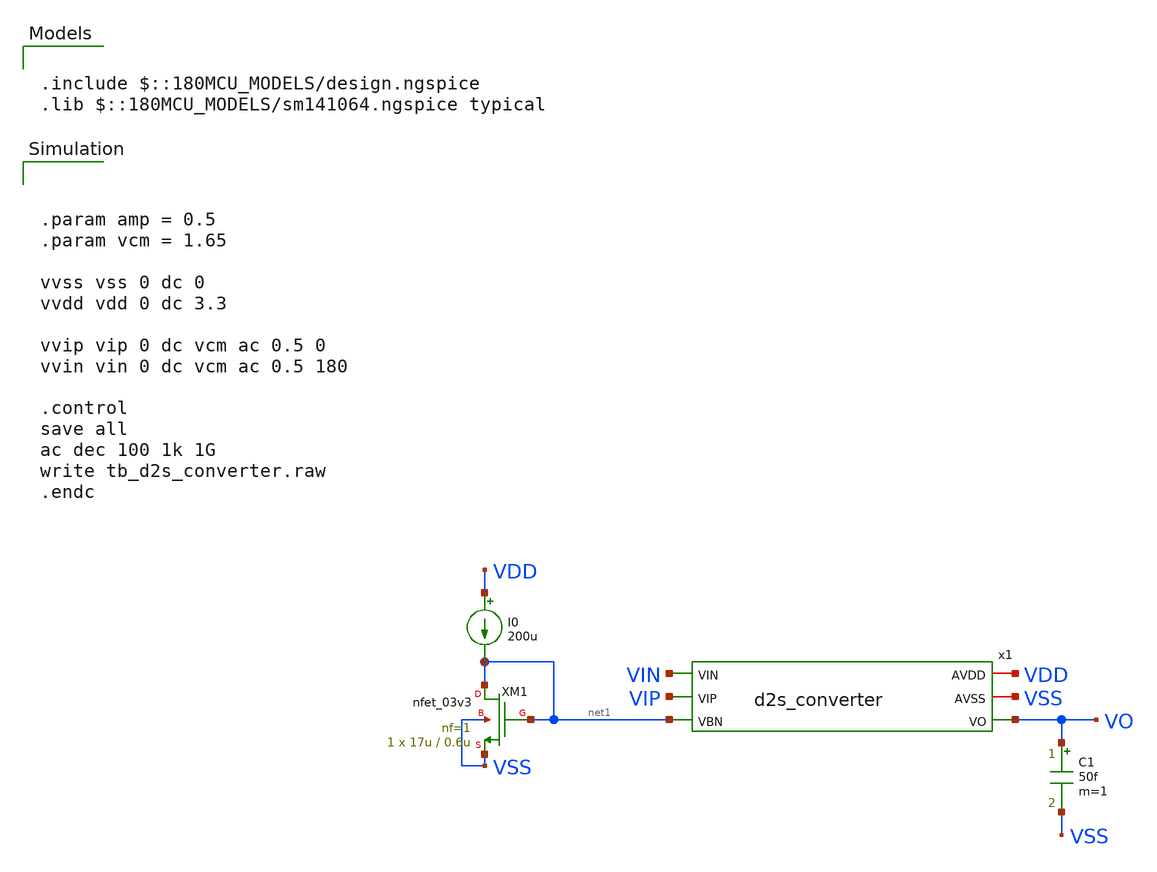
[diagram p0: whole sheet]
** sch_path: designs/libs/tb_analog/tb_d2s_converter/tb_d2s_converter.sch
**.subckt tb_d2s_converter
XM1 net1 net1 VSS VSS nfet_03v3 L=0.6u W=17u nf=1 ad='int((nf+1)/2) * W/nf * 0.18u' as='int((nf+2)/2) * W/nf * 0.18u'
+ pd='2*int((nf+1)/2) * (W/nf + 0.18u)' ps='2*int((nf+2)/2) * (W/nf + 0.18u)' nrd='0.18u / W' nrs='0.18u / W'
+ sa=0 sb=0 sd=0 m=1
I0 VDD net1 200u
C1 VO VSS 50f m=1
x1 VDD VSS VIN VIP net1 VO d2s_converter
**** begin user architecture code



.param amp = 0.5
.param vcm = 1.65

vvss vss 0 dc 0
vvdd vdd 0 dc 3.3

vvip vip 0 dc vcm ac 0.5 0
vvin vin 0 dc vcm ac 0.5 180

.control
save all
ac dec 100 1k 1G
write tb_d2s_converter.raw
.endc



.include $::180MCU_MODELS/design.ngspice
.lib $::180MCU_MODELS/sm141064.ngspice typical

**** end user architecture code
**.ends

* expanding   symbol:  libs/core_analog/d2s_converter/d2s_converter.sym # of pins=6
** sym_path: designs/libs/core_analog/d2s_converter/d2s_converter.sym
** sch_path: designs/libs/core_analog/d2s_converter/d2s_converter.sch
.subckt d2s_converter AVDD AVSS VIN VIP VBN VO
*.iopin AVDD
*.iopin AVSS
*.ipin VIN
*.ipin VIP
*.opin VO
*.ipin VBN
XM2 VOPB VIN i1 AVSS nfet_03v3 L=0.3u W=1.9u nf=1 ad='int((nf+1)/2) * W/nf * 0.18u' as='int((nf+2)/2) * W/nf * 0.18u'
+ pd='2*int((nf+1)/2) * (W/nf + 0.18u)' ps='2*int((nf+2)/2) * (W/nf + 0.18u)' nrd='0.18u / W' nrs='0.18u / W'
+ sa=0 sb=0 sd=0 m=4
XM4 VOPB VOPB AVDD AVDD pfet_03v3 L=0.3u W=1.4u nf=1 ad='int((nf+1)/2) * W/nf * 0.18u' as='int((nf+2)/2) * W/nf * 0.18u'
+ pd='2*int((nf+1)/2) * (W/nf + 0.18u)' ps='2*int((nf+2)/2) * (W/nf + 0.18u)' nrd='0.18u / W' nrs='0.18u / W'
+ sa=0 sb=0 sd=0 m=4
XM11 VOB VOB AVSS AVSS nfet_03v3 L=0.3u W=1.5u nf=1 ad='int((nf+1)/2) * W/nf * 0.18u' as='int((nf+2)/2) * W/nf * 0.18u'
+ pd='2*int((nf+1)/2) * (W/nf + 0.18u)' ps='2*int((nf+2)/2) * (W/nf + 0.18u)' nrd='0.18u / W' nrs='0.18u / W'
+ sa=0 sb=0 sd=0 m=4
XM13 VOB VOP AVDD AVDD pfet_03v3 L=0.3u W=2u nf=1 ad='int((nf+1)/2) * W/nf * 0.18u' as='int((nf+2)/2) * W/nf * 0.18u'
+ pd='2*int((nf+1)/2) * (W/nf + 0.18u)' ps='2*int((nf+2)/2) * (W/nf + 0.18u)' nrd='0.18u / W' nrs='0.18u / W'
+ sa=0 sb=0 sd=0 m=4
XM3 VOP VIP i1 AVSS nfet_03v3 L=0.3u W=1.9u nf=1 ad='int((nf+1)/2) * W/nf * 0.18u' as='int((nf+2)/2) * W/nf * 0.18u'
+ pd='2*int((nf+1)/2) * (W/nf + 0.18u)' ps='2*int((nf+2)/2) * (W/nf + 0.18u)' nrd='0.18u / W' nrs='0.18u / W'
+ sa=0 sb=0 sd=0 m=4
XM5 VOP VOPB AVDD AVDD pfet_03v3 L=0.3u W=1.4u nf=1 ad='int((nf+1)/2) * W/nf * 0.18u' as='int((nf+2)/2) * W/nf * 0.18u'
+ pd='2*int((nf+1)/2) * (W/nf + 0.18u)' ps='2*int((nf+2)/2) * (W/nf + 0.18u)' nrd='0.18u / W' nrs='0.18u / W'
+ sa=0 sb=0 sd=0 m=4
XM7 VONB VIP i2 AVSS nfet_03v3 L=0.3u W=1.9u nf=1 ad='int((nf+1)/2) * W/nf * 0.18u' as='int((nf+2)/2) * W/nf * 0.18u'
+ pd='2*int((nf+1)/2) * (W/nf + 0.18u)' ps='2*int((nf+2)/2) * (W/nf + 0.18u)' nrd='0.18u / W' nrs='0.18u / W'
+ sa=0 sb=0 sd=0 m=4
XM8 VONB VONB AVDD AVDD pfet_03v3 L=0.3u W=1.4u nf=1 ad='int((nf+1)/2) * W/nf * 0.18u' as='int((nf+2)/2) * W/nf * 0.18u'
+ pd='2*int((nf+1)/2) * (W/nf + 0.18u)' ps='2*int((nf+2)/2) * (W/nf + 0.18u)' nrd='0.18u / W' nrs='0.18u / W'
+ sa=0 sb=0 sd=0 m=4
XM9 VON VIN i2 AVSS nfet_03v3 L=0.3u W=1.9u nf=1 ad='int((nf+1)/2) * W/nf * 0.18u' as='int((nf+2)/2) * W/nf * 0.18u'
+ pd='2*int((nf+1)/2) * (W/nf + 0.18u)' ps='2*int((nf+2)/2) * (W/nf + 0.18u)' nrd='0.18u / W' nrs='0.18u / W'
+ sa=0 sb=0 sd=0 m=4
XM10 VON VONB AVDD AVDD pfet_03v3 L=0.3u W=1.4u nf=1 ad='int((nf+1)/2) * W/nf * 0.18u' as='int((nf+2)/2) * W/nf * 0.18u'
+ pd='2*int((nf+1)/2) * (W/nf + 0.18u)' ps='2*int((nf+2)/2) * (W/nf + 0.18u)' nrd='0.18u / W' nrs='0.18u / W'
+ sa=0 sb=0 sd=0 m=4
XM14 VO VON AVDD AVDD pfet_03v3 L=0.3u W=2u nf=1 ad='int((nf+1)/2) * W/nf * 0.18u' as='int((nf+2)/2) * W/nf * 0.18u'
+ pd='2*int((nf+1)/2) * (W/nf + 0.18u)' ps='2*int((nf+2)/2) * (W/nf + 0.18u)' nrd='0.18u / W' nrs='0.18u / W'
+ sa=0 sb=0 sd=0 m=4
XM12 VO VOB AVSS AVSS nfet_03v3 L=0.3u W=1.5u nf=1 ad='int((nf+1)/2) * W/nf * 0.18u' as='int((nf+2)/2) * W/nf * 0.18u'
+ pd='2*int((nf+1)/2) * (W/nf + 0.18u)' ps='2*int((nf+2)/2) * (W/nf + 0.18u)' nrd='0.18u / W' nrs='0.18u / W'
+ sa=0 sb=0 sd=0 m=4
XM1 i1 VBN AVSS AVSS nfet_03v3 L=0.5u W=11.25u nf=1 ad='int((nf+1)/2) * W/nf * 0.18u' as='int((nf+2)/2) * W/nf * 0.18u'
+ pd='2*int((nf+1)/2) * (W/nf + 0.18u)' ps='2*int((nf+2)/2) * (W/nf + 0.18u)' nrd='0.18u / W' nrs='0.18u / W'
+ sa=0 sb=0 sd=0 m=4
XM6 i2 VBN AVSS AVSS nfet_03v3 L=0.5u W=11.25u nf=1 ad='int((nf+1)/2) * W/nf * 0.18u' as='int((nf+2)/2) * W/nf * 0.18u'
+ pd='2*int((nf+1)/2) * (W/nf + 0.18u)' ps='2*int((nf+2)/2) * (W/nf + 0.18u)' nrd='0.18u / W' nrs='0.18u / W'
+ sa=0 sb=0 sd=0 m=4
.ends

.end
